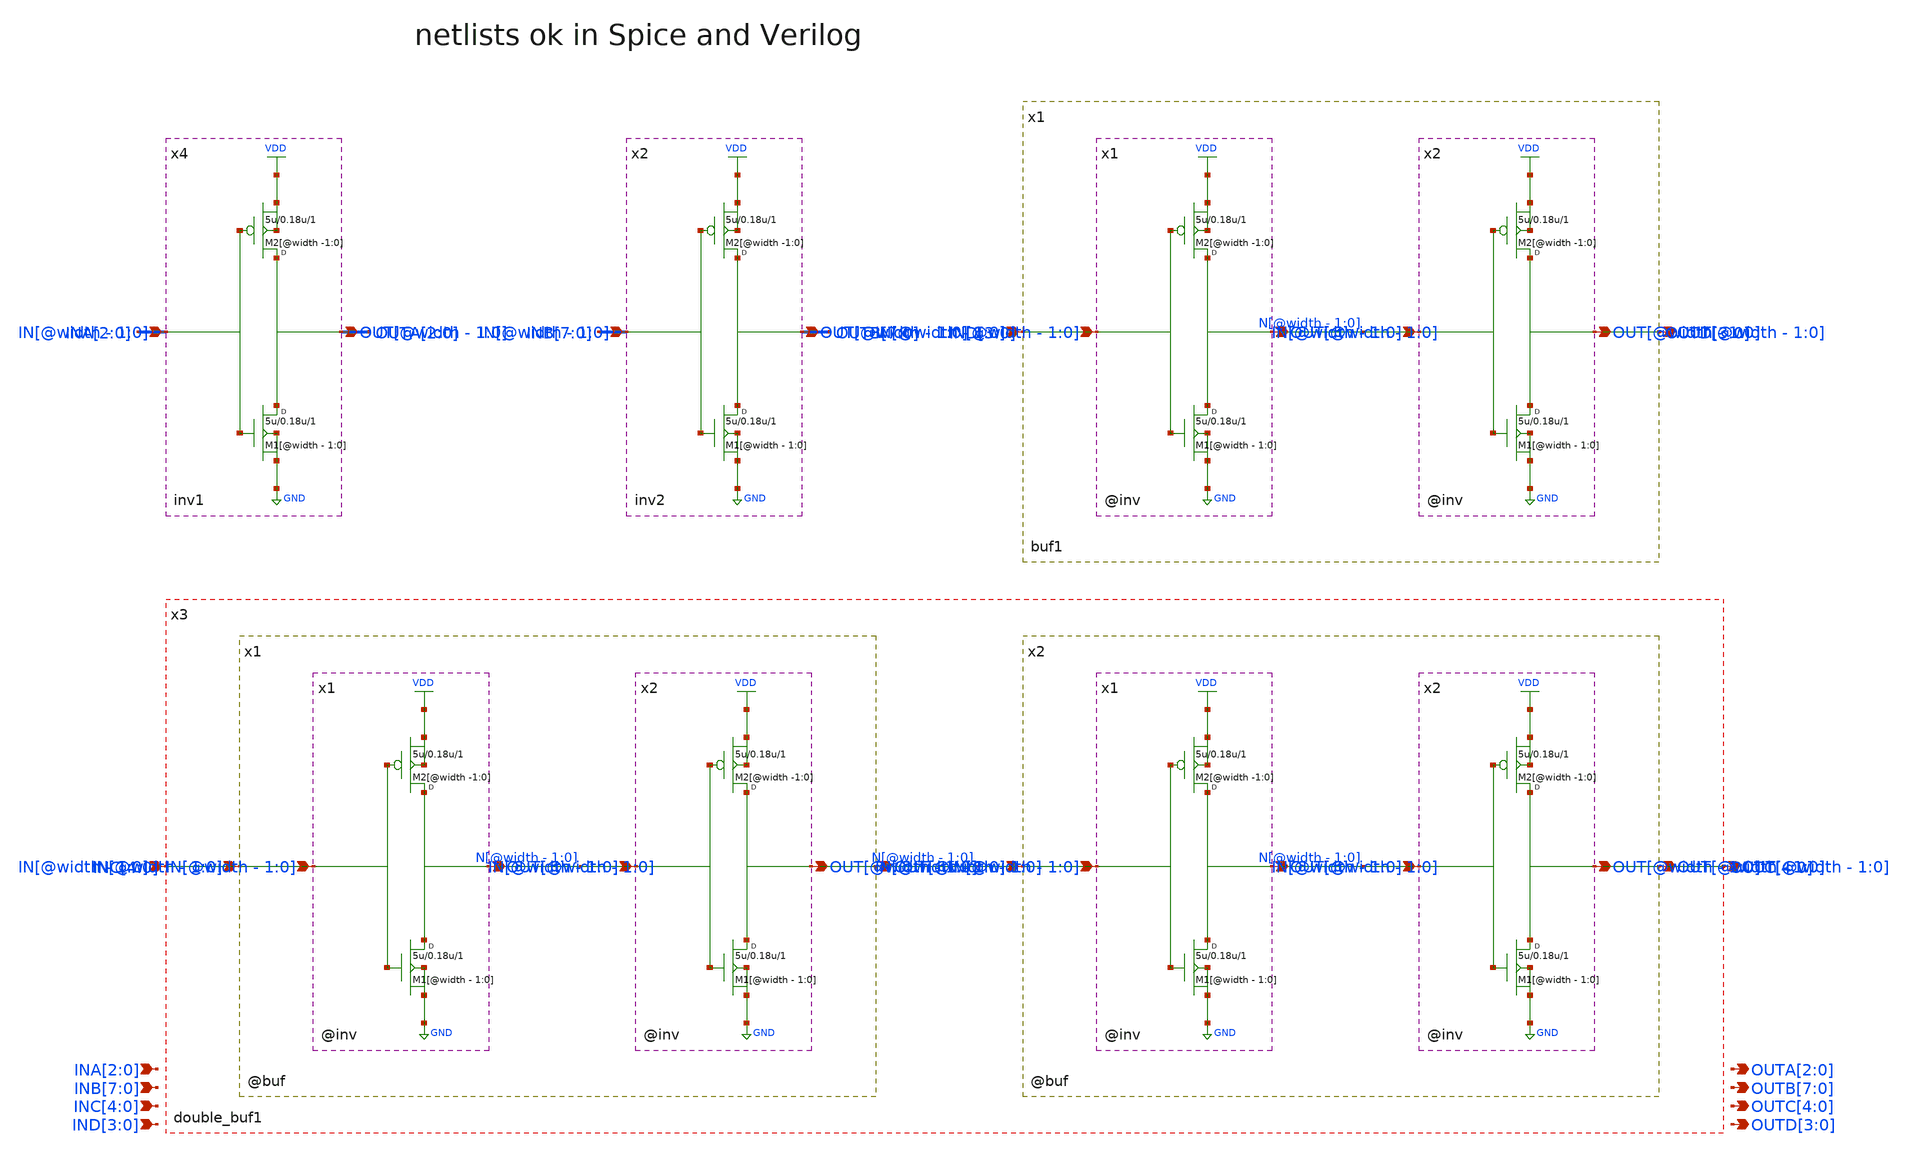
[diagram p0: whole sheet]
** sch_path: xschem_library/examples/test_parametric_ports/tb_param_ports_lcc.sch
**.subckt tb_param_ports_lcc IND[3],IND[2],IND[1],IND[0] INC[4],INC[3],INC[2],INC[1],INC[0]
*+ INB[7],INB[6],INB[5],INB[4],INB[3],INB[2],INB[1],INB[0] INA[2],INA[1],INA[0] OUTD[3],OUTD[2],OUTD[1],OUTD[0] OUTC[4],OUTC[3],OUTC[2],OUTC[1],OUTC[0]
*+ OUTB[7],OUTB[6],OUTB[5],OUTB[4],OUTB[3],OUTB[2],OUTB[1],OUTB[0] OUTA[2],OUTA[1],OUTA[0]
*.ipin IND[3],IND[2],IND[1],IND[0]
*.ipin INC[4],INC[3],INC[2],INC[1],INC[0]
*.ipin INB[7],INB[6],INB[5],INB[4],INB[3],INB[2],INB[1],INB[0]
*.ipin INA[2],INA[1],INA[0]
*.opin OUTD[3],OUTD[2],OUTD[1],OUTD[0]
*.opin OUTC[4],OUTC[3],OUTC[2],OUTC[1],OUTC[0]
*.opin OUTB[7],OUTB[6],OUTB[5],OUTB[4],OUTB[3],OUTB[2],OUTB[1],OUTB[0]
*.opin OUTA[2],OUTA[1],OUTA[0]
x2 OUTB[7] OUTB[6] OUTB[5] OUTB[4] OUTB[3] OUTB[2] OUTB[1] OUTB[0] INB[7] INB[6] INB[5] INB[4]
+ INB[3] INB[2] INB[1] INB[0] inv2
x4 OUTA[2] OUTA[1] OUTA[0] INA[2] INA[1] INA[0] inv1
x1 OUTD[3] OUTD[2] OUTD[1] OUTD[0] IND[3] IND[2] IND[1] IND[0] buf1
x3 OUTC[4] OUTC[3] OUTC[2] OUTC[1] OUTC[0] INC[4] INC[3] INC[2] INC[1] INC[0] double_buf1
**.ends
.end
